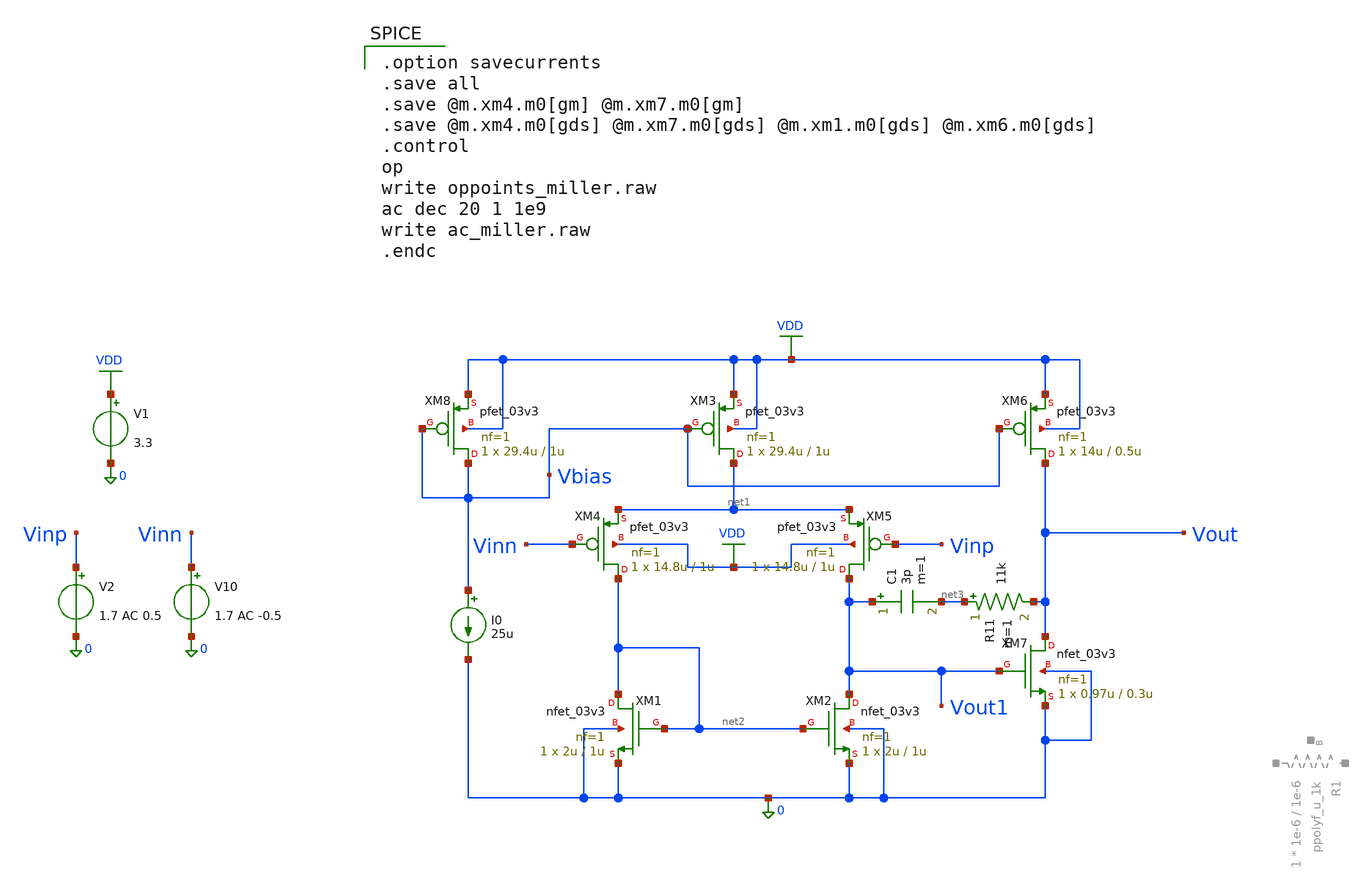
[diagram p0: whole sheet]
** sch_path: jz_tia/two_stage_miller_larger.sch
**.subckt two_stage_miller_larger
XM1 net2 net2 0 0 nfet_03v3 L=1u W=2u nf=1 ad='int((nf+1)/2) * W/nf * 0.18u' as='int((nf+2)/2) * W/nf * 0.18u'
+ pd='2*int((nf+1)/2) * (W/nf + 0.18u)' ps='2*int((nf+2)/2) * (W/nf + 0.18u)' nrd='0.18u / W' nrs='0.18u / W'
+ sa=0 sb=0 sd=0 m=1
XM2 Vout1 net2 0 0 nfet_03v3 L=1u W=2u nf=1 ad='int((nf+1)/2) * W/nf * 0.18u' as='int((nf+2)/2) * W/nf * 0.18u'
+ pd='2*int((nf+1)/2) * (W/nf + 0.18u)' ps='2*int((nf+2)/2) * (W/nf + 0.18u)' nrd='0.18u / W' nrs='0.18u / W'
+ sa=0 sb=0 sd=0 m=1
XM3 net1 Vbias VDD VDD pfet_03v3 L=1u W=29.4u nf=1 ad='int((nf+1)/2) * W/nf * 0.18u' as='int((nf+2)/2) * W/nf * 0.18u'
+ pd='2*int((nf+1)/2) * (W/nf + 0.18u)' ps='2*int((nf+2)/2) * (W/nf + 0.18u)' nrd='0.18u / W' nrs='0.18u / W'
+ sa=0 sb=0 sd=0 m=1
XM4 net2 Vinn net1 VDD pfet_03v3 L=1u W=14.8u nf=1 ad='int((nf+1)/2) * W/nf * 0.18u' as='int((nf+2)/2) * W/nf * 0.18u'
+ pd='2*int((nf+1)/2) * (W/nf + 0.18u)' ps='2*int((nf+2)/2) * (W/nf + 0.18u)' nrd='0.18u / W' nrs='0.18u / W'
+ sa=0 sb=0 sd=0 m=1
XM5 Vout1 Vinp net1 VDD pfet_03v3 L=1u W=14.8u nf=1 ad='int((nf+1)/2) * W/nf * 0.18u' as='int((nf+2)/2) * W/nf * 0.18u'
+ pd='2*int((nf+1)/2) * (W/nf + 0.18u)' ps='2*int((nf+2)/2) * (W/nf + 0.18u)' nrd='0.18u / W' nrs='0.18u / W'
+ sa=0 sb=0 sd=0 m=1
XM6 Vout Vbias VDD VDD pfet_03v3 L=0.5u W=14u nf=1 ad='int((nf+1)/2) * W/nf * 0.18u' as='int((nf+2)/2) * W/nf * 0.18u'
+ pd='2*int((nf+1)/2) * (W/nf + 0.18u)' ps='2*int((nf+2)/2) * (W/nf + 0.18u)' nrd='0.18u / W' nrs='0.18u / W'
+ sa=0 sb=0 sd=0 m=1
XM7 Vout Vout1 0 0 nfet_03v3 L=0.3u W=0.97u nf=1 ad='int((nf+1)/2) * W/nf * 0.18u' as='int((nf+2)/2) * W/nf * 0.18u'
+ pd='2*int((nf+1)/2) * (W/nf + 0.18u)' ps='2*int((nf+2)/2) * (W/nf + 0.18u)' nrd='0.18u / W' nrs='0.18u / W'
+ sa=0 sb=0 sd=0 m=1
XM8 Vbias Vbias VDD VDD pfet_03v3 L=1u W=29.4u nf=1 ad='int((nf+1)/2) * W/nf * 0.18u' as='int((nf+2)/2) * W/nf * 0.18u'
+ pd='2*int((nf+1)/2) * (W/nf + 0.18u)' ps='2*int((nf+2)/2) * (W/nf + 0.18u)' nrd='0.18u / W' nrs='0.18u / W'
+ sa=0 sb=0 sd=0 m=1
I0 Vbias 0 25u
V2 Vinp 0 1.7 AC 0.5
V10 Vinn 0 1.7 AC -0.5
V1 VDD 0 3.3
C1 Vout1 net3 3p m=1
R11 net3 Vout 11k m=1
**** begin user architecture code

.include $::180MCU_MODELS/design.ngspice
.lib $::180MCU_MODELS/sm141064.ngspice typical
.lib $::180MCU_MODELS/smbb000149.ngspice typical


.option savecurrents
.save all
.save @m.xm4.m0[gm] @m.xm7.m0[gm]
.save @m.xm4.m0[gds] @m.xm7.m0[gds] @m.xm1.m0[gds] @m.xm6.m0[gds]
.control
op
write oppoints_miller.raw
ac dec 20 1 1e9
write ac_miller.raw
.endc

**** end user architecture code
**.ends
.GLOBAL VDD
.end
